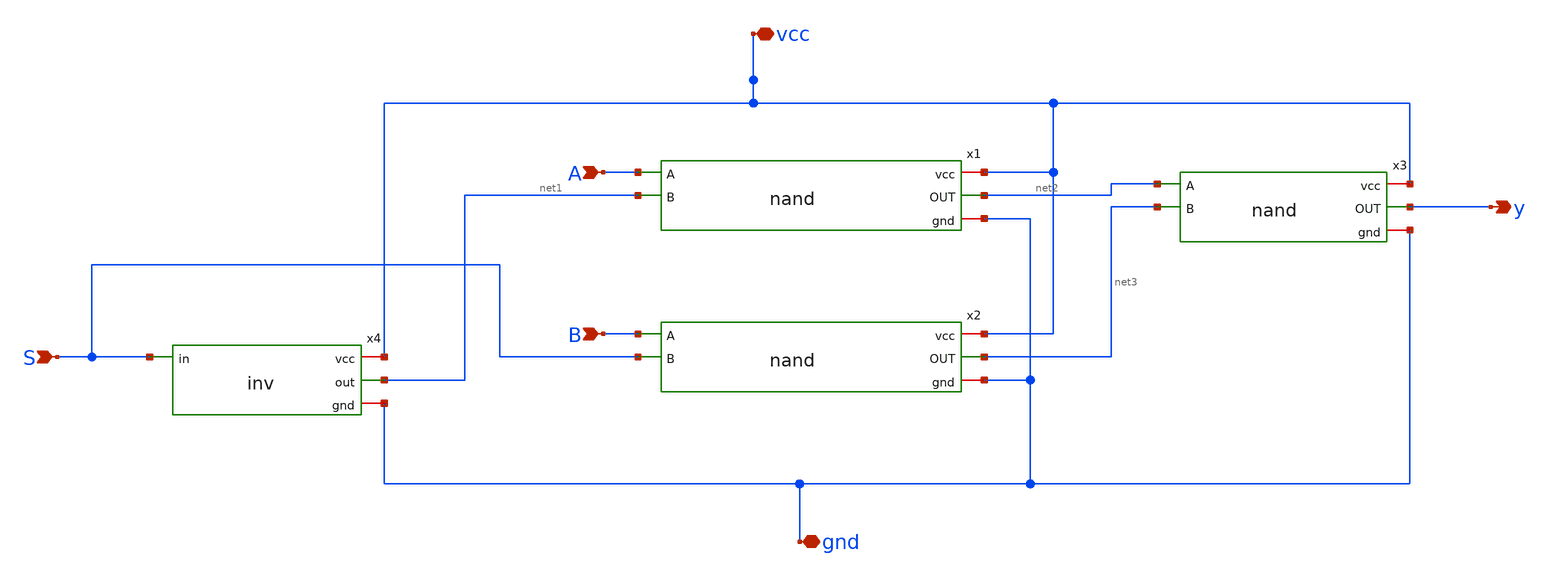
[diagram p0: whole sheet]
** sch_path: designs/schematics/mux2x1/mux_nand.sch
**.subckt mux_nand S A B y vcc gnd
*.ipin S
*.ipin A
*.ipin B
*.opin y
*.iopin vcc
*.iopin gnd
x4 vcc S net1 gnd inv
x1 vcc net2 A net1 gnd nand
x2 vcc net3 B S gnd nand
x3 vcc y net2 net3 gnd nand
**.ends

* expanding   symbol:  voidwalkers-scandff-gf180mcu/designs/schematics/mux2x1/inv.sym # of pins=4
** sym_path: designs/schematics/mux2x1/inv.sym
** sch_path: designs/schematics/mux2x1/inv.sch
.subckt inv vcc in out gnd
*.ipin in
*.opin out
*.iopin vcc
*.iopin gnd
XM2 out in vcc vcc pfet_03v3 L=0.28u W=0.22u nf=1 ad='int((nf+1)/2) * W/nf * 0.18u' as='int((nf+2)/2) * W/nf * 0.18u'
+ pd='2*int((nf+1)/2) * (W/nf + 0.18u)' ps='2*int((nf+2)/2) * (W/nf + 0.18u)' nrd='0.18u / W' nrs='0.18u / W'
+ sa=0 sb=0 sd=0 m=1
XM1 out in gnd gnd nfet_03v3 L=0.28u W=0.22u nf=1 ad='int((nf+1)/2) * W/nf * 0.18u' as='int((nf+2)/2) * W/nf * 0.18u'
+ pd='2*int((nf+1)/2) * (W/nf + 0.18u)' ps='2*int((nf+2)/2) * (W/nf + 0.18u)' nrd='0.18u / W' nrs='0.18u / W'
+ sa=0 sb=0 sd=0 m=1
.ends


* expanding   symbol:  voidwalkers-scandff-gf180mcu/designs/schematics/mux2x1/nand.sym # of pins=5
** sym_path: designs/schematics/mux2x1/nand.sym
** sch_path: designs/schematics/mux2x1/nand.sch
.subckt nand vcc OUT A B gnd
*.ipin A
*.ipin B
*.opin OUT
*.iopin vcc
*.iopin gnd
XM1 OUT B net1 gnd nfet_03v3 L=0.28u W=0.22u nf=1 ad='int((nf+1)/2) * W/nf * 0.18u' as='int((nf+2)/2) * W/nf * 0.18u'
+ pd='2*int((nf+1)/2) * (W/nf + 0.18u)' ps='2*int((nf+2)/2) * (W/nf + 0.18u)' nrd='0.18u / W' nrs='0.18u / W'
+ sa=0 sb=0 sd=0 m=1
XM2 net1 A gnd gnd nfet_03v3 L=0.28u W=0.22u nf=1 ad='int((nf+1)/2) * W/nf * 0.18u' as='int((nf+2)/2) * W/nf * 0.18u'
+ pd='2*int((nf+1)/2) * (W/nf + 0.18u)' ps='2*int((nf+2)/2) * (W/nf + 0.18u)' nrd='0.18u / W' nrs='0.18u / W'
+ sa=0 sb=0 sd=0 m=1
XM3 OUT A vcc vcc pfet_03v3 L=0.28u W=0.22u nf=1 ad='int((nf+1)/2) * W/nf * 0.18u' as='int((nf+2)/2) * W/nf * 0.18u'
+ pd='2*int((nf+1)/2) * (W/nf + 0.18u)' ps='2*int((nf+2)/2) * (W/nf + 0.18u)' nrd='0.18u / W' nrs='0.18u / W'
+ sa=0 sb=0 sd=0 m=1
XM4 OUT B vcc vcc pfet_03v3 L=0.28u W=0.22u nf=1 ad='int((nf+1)/2) * W/nf * 0.18u' as='int((nf+2)/2) * W/nf * 0.18u'
+ pd='2*int((nf+1)/2) * (W/nf + 0.18u)' ps='2*int((nf+2)/2) * (W/nf + 0.18u)' nrd='0.18u / W' nrs='0.18u / W'
+ sa=0 sb=0 sd=0 m=1
.ends

.end
